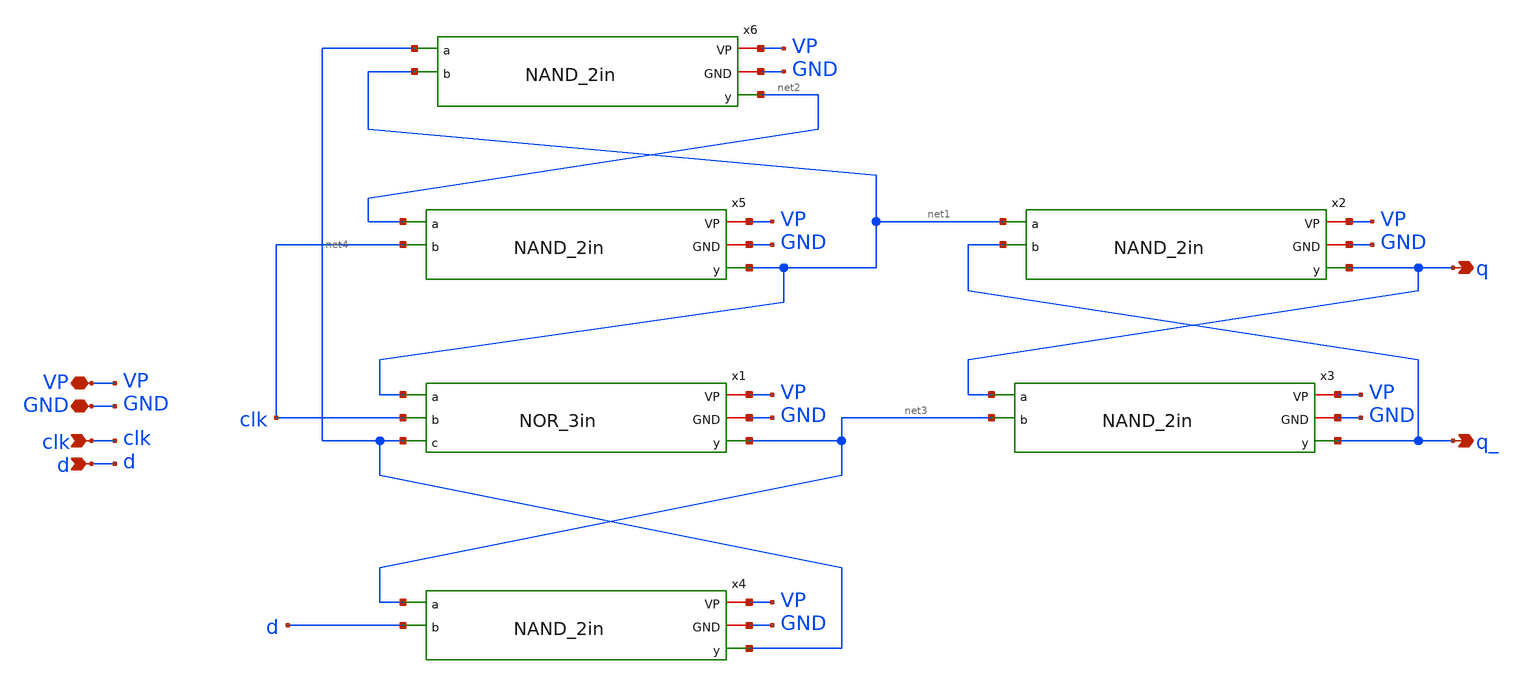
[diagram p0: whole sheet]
** sch_path: schematics/divider/schematics/d_flip_flop.sch
**.subckt d_flip_flop GND clk VP d q q_
*.iopin GND
*.ipin clk
*.iopin VP
*.ipin d
*.opin q
*.opin q_
x2 VP GND net1 q q_ NAND_2in
x3 VP GND q q_ net3 NAND_2in
x4 VP GND net3 net4 d NAND_2in
x5 VP GND net2 net1 clk NAND_2in
x6 VP GND net4 net2 net1 NAND_2in
x1 VP GND net1 net3 clk net4 NOR_3in
**.ends
.end
